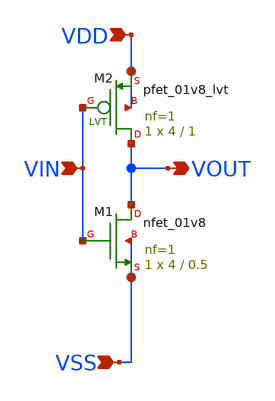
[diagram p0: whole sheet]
** sch_path: design/LELO_SVOD_SKY130A/LELO_INV_PVT.sch
**.subckt LELO_INV_PVT VIN VDD VSS VOUT
*.ipin VIN
*.ipin VDD
*.ipin VSS
*.opin VOUT
XM1 VOUT VIN VSS VSS sky130_fd_pr__nfet_01v8 L=0.5 W=4 nf=1 ad='int((1 + 1)/2) * 4 / 1 * 0.29' as='int((1 + 2)/2) * 4 / 1 * 0.29'
+ pd='2*int((1 + 1)/2) * (4 / 1 + 0.29)' ps='2*int((1 + 2)/2) * (4 / 1 + 0.29)' nrd='0.29 / 4 ' nrs='0.29 / 4 '
+ sa=0 sb=0 sd=0 mult=1 m=1
XM2 VOUT VIN VDD VDD sky130_fd_pr__pfet_01v8_lvt L=1 W=4 nf=1 ad='int((1 + 1)/2) * 4 / 1 * 0.29' as='int((1 + 2)/2) * 4 / 1 * 0.29'
+ pd='2*int((1 + 1)/2) * (4 / 1 + 0.29)' ps='2*int((1 + 2)/2) * (4 / 1 + 0.29)' nrd='0.29 / 4 ' nrs='0.29 / 4 '
+ sa=0 sb=0 sd=0 mult=1 m=1
**.ends
.end
